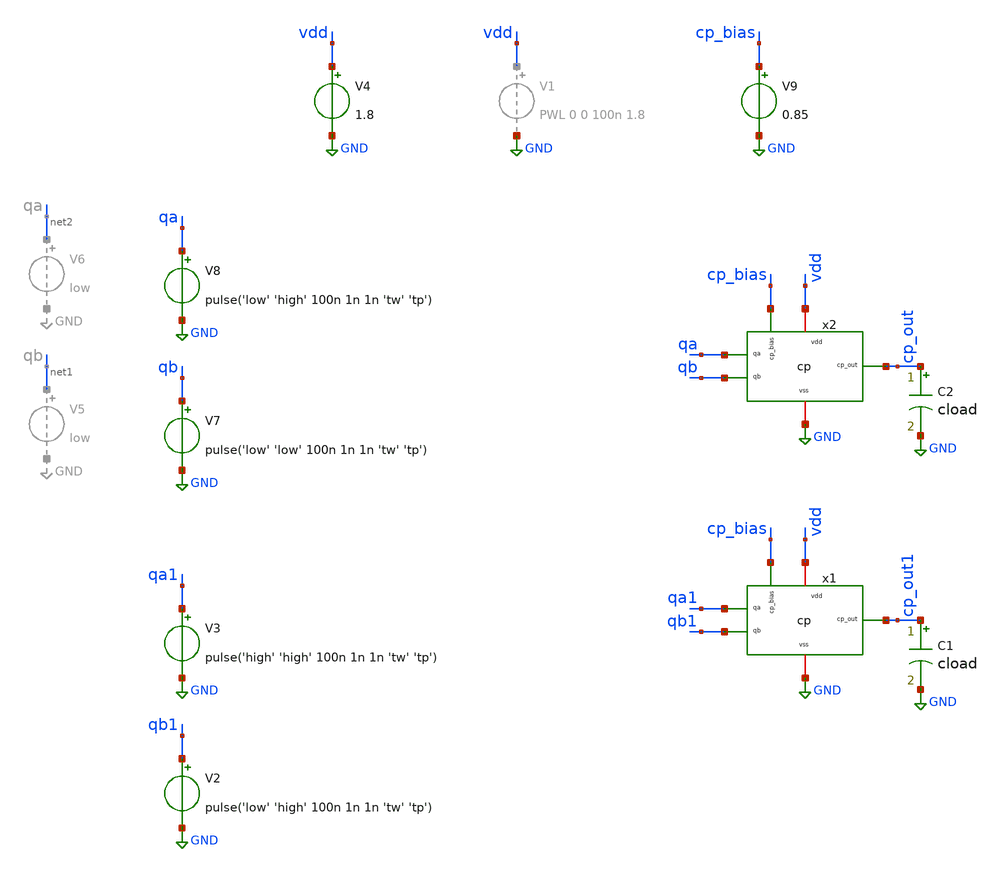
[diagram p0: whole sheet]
** sch_path: xschem01/cp/cp_tran.sch
**.subckt cp_tran
x1 vdd qa1 cp_out1 qb1 GND cp_bias cp
V2 qb1 GND pulse('low' 'high' 100n 1n 1n 'tw' 'tp')
V3 qa1 GND pulse('high' 'high' 100n 1n 1n 'tw' 'tp')
C1 cp_out1 GND cload m=1
V4 vdd GND 1.8
V7 qb GND pulse('low' 'low' 100n 1n 1n 'tw' 'tp')
V8 qa GND pulse('low' 'high' 100n 1n 1n 'tw' 'tp')
x2 vdd qa cp_out qb GND cp_bias cp
C2 cp_out GND cload m=1
V9 cp_bias GND 0.85
**** begin user architecture code


.options acct list savecurrents
.temp 25
.param cload=5p  ibias=10u  low=0  high=1.8  tw=40n  tp=80n
******charging
*+ tw_a=50n tp_a=80n
*+ tw_b=0n  tp_b=0n
******discharging
*+ tw_a=0n tp_a=0n
*+ tw_b=50n  tp_b=80n

.include /usr/local/share/pdk/sky130A/libs.ref/sky130_fd_sc_hd/spice/sky130_fd_sc_hd.spice

.ic v(cp_out)=1.8  v(cp_out1)=1.8

*.meas tran TRAN_PERIOD TRIG V(QA) VAL=0.5 RISE=1 TARG V(QA) VAL=0.5 RISE=2
*.meas tran TRAN_FREQ param='1/TRAN_PERIOD'

.print TRAN_PERIOD  TRAN_FREQ
*print @m.x1.xm3.msky130_fd_pr__nfet_01v8[id]  @m.x1.xm4.msky130_fd_pr__pfet_01v8[id]


.control
save all
save @m.x1.xm3.msky130_fd_pr__nfet_01v8[vth]
save @m.x1.xm3.msky130_fd_pr__nfet_01v8[vgs]
save @m.x1.xm3.msky130_fd_pr__nfet_01v8[gm]

save @m.x1.xm6.msky130_fd_pr__pfet_01v8[vth]

save @m.x1.xm4.msky130_fd_pr__pfet_01v8[vsg]
save @m.x1.xm6.msky130_fd_pr__pfet_01v8[vsg]


op
write cp_tran.raw
set appendwrite

tran 1n 10u
write cp_tran.raw

print  @m.x1.xm3.msky130_fd_pr__nfet_01v8[vth]
print  @m.x1.xm3.msky130_fd_pr__nfet_01v8[gm]
print  @m.x1.xm3.msky130_fd_pr__nfet_01v8[vgs]

*print x1.bias  x1.n1   x1.cp_out

.endc



** opencircuitdesign pdks install
.lib $::SKYWATER_MODELS/sky130.lib.spice tt


**** end user architecture code
**.ends

* expanding   symbol:  cp/cp.sym # of pins=6
** sym_path: cp/cp.sym
** sch_path: cp/cp.sch
.subckt cp vdd qa cp_out qb vss cp_bias
*.ipin qa
*.ipin qb
*.opin cp_out
*.iopin vdd
*.iopin vss
*.ipin cp_bias
XM1 n1 n1 vdd vdd sky130_fd_pr__pfet_01v8 L=0.15 W=2 nf=1 ad='int((nf+1)/2) * W/nf * 0.29' as='int((nf+2)/2) * W/nf * 0.29'
+ pd='2*int((nf+1)/2) * (W/nf + 0.29)' ps='2*int((nf+2)/2) * (W/nf + 0.29)' nrd='0.29 / W' nrs='0.29 / W'
+ sa=0 sb=0 sd=0 mult=1 m=1
XM2 net3 bias vss vss sky130_fd_pr__nfet_01v8 L=0.3 W=1 nf=1 ad='int((nf+1)/2) * W/nf * 0.29' as='int((nf+2)/2) * W/nf * 0.29'
+ pd='2*int((nf+1)/2) * (W/nf + 0.29)' ps='2*int((nf+2)/2) * (W/nf + 0.29)' nrd='0.29 / W' nrs='0.29 / W'
+ sa=0 sb=0 sd=0 mult=1 m=1
XM3 bias bias vss vss sky130_fd_pr__nfet_01v8 L=0.30 W=1 nf=1 ad='int((nf+1)/2) * W/nf * 0.29' as='int((nf+2)/2) * W/nf * 0.29'
+ pd='2*int((nf+1)/2) * (W/nf + 0.29)' ps='2*int((nf+2)/2) * (W/nf + 0.29)' nrd='0.29 / W' nrs='0.29 / W'
+ sa=0 sb=0 sd=0 mult=1 m=1
XM4 n2 n1 vdd vdd sky130_fd_pr__pfet_01v8 L=0.15 W=2 nf=1 ad='int((nf+1)/2) * W/nf * 0.29' as='int((nf+2)/2) * W/nf * 0.29'
+ pd='2*int((nf+1)/2) * (W/nf + 0.29)' ps='2*int((nf+2)/2) * (W/nf + 0.29)' nrd='0.29 / W' nrs='0.29 / W'
+ sa=0 sb=0 sd=0 mult=1 m=1
XM5 n3 bias vss vss sky130_fd_pr__nfet_01v8 L=0.3 W=1 nf=1 ad='int((nf+1)/2) * W/nf * 0.29' as='int((nf+2)/2) * W/nf * 0.29'
+ pd='2*int((nf+1)/2) * (W/nf + 0.29)' ps='2*int((nf+2)/2) * (W/nf + 0.29)' nrd='0.29 / W' nrs='0.29 / W'
+ sa=0 sb=0 sd=0 mult=1 m=1
XM6 cp_out qa net4 vdd sky130_fd_pr__pfet_01v8 L=0.15 W=2 nf=1 ad='int((nf+1)/2) * W/nf * 0.29' as='int((nf+2)/2) * W/nf * 0.29'
+ pd='2*int((nf+1)/2) * (W/nf + 0.29)' ps='2*int((nf+2)/2) * (W/nf + 0.29)' nrd='0.29 / W' nrs='0.29 / W'
+ sa=0 sb=0 sd=0 mult=1 m=1
XM7 net2 qb n3 vss sky130_fd_pr__nfet_01v8 L=0.3 W=1 nf=1 ad='int((nf+1)/2) * W/nf * 0.29' as='int((nf+2)/2) * W/nf * 0.29'
+ pd='2*int((nf+1)/2) * (W/nf + 0.29)' ps='2*int((nf+2)/2) * (W/nf + 0.29)' nrd='0.29 / W' nrs='0.29 / W'
+ sa=0 sb=0 sd=0 mult=1 m=1
XM8 net1 cp_bias vdd vdd sky130_fd_pr__pfet_01v8 L=0.15 W=2 nf=1 ad='int((nf+1)/2) * W/nf * 0.29' as='int((nf+2)/2) * W/nf * 0.29'
+ pd='2*int((nf+1)/2) * (W/nf + 0.29)' ps='2*int((nf+2)/2) * (W/nf + 0.29)' nrd='0.29 / W' nrs='0.29 / W'
+ sa=0 sb=0 sd=0 mult=1 m=1
Vmeas n2 net4 0
.save i(vmeas)
Vmeas2 cp_out net2 0
.save i(vmeas2)
Vmeas3 n1 net3 0
.save i(vmeas3)
Vmeas4 net1 bias 0
.save i(vmeas4)
.ends

.GLOBAL GND
.end
